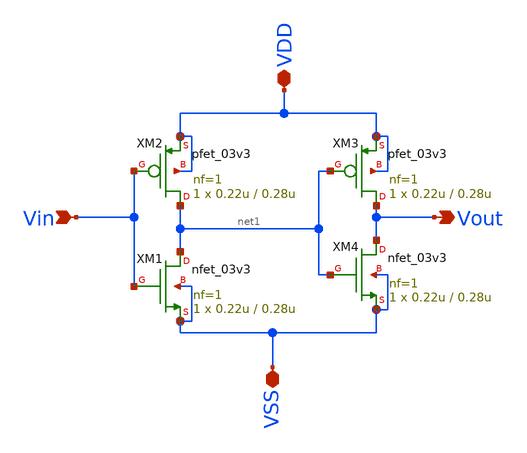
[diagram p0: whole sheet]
** sch_path: analog/top/buffer.sch
**.subckt buffer Vin Vout VSS VDD
*.ipin Vin
*.opin Vout
*.iopin VSS
*.iopin VDD
XM1 net1 Vin VSS VSS nfet_03v3 L=0.28u W=0.22u nf=1 ad='int((nf+1)/2) * W/nf * 0.18u' as='int((nf+2)/2) * W/nf * 0.18u'
+ pd='2*int((nf+1)/2) * (W/nf + 0.18u)' ps='2*int((nf+2)/2) * (W/nf + 0.18u)' nrd='0.18u / W' nrs='0.18u / W'
+ sa=0 sb=0 sd=0 m=1
XM2 net1 Vin VDD VDD pfet_03v3 L=0.28u W=0.22u nf=1 ad='int((nf+1)/2) * W/nf * 0.18u' as='int((nf+2)/2) * W/nf * 0.18u'
+ pd='2*int((nf+1)/2) * (W/nf + 0.18u)' ps='2*int((nf+2)/2) * (W/nf + 0.18u)' nrd='0.18u / W' nrs='0.18u / W'
+ sa=0 sb=0 sd=0 m=1
XM3 Vout net1 VDD VDD pfet_03v3 L=0.28u W=0.22u nf=1 ad='int((nf+1)/2) * W/nf * 0.18u' as='int((nf+2)/2) * W/nf * 0.18u'
+ pd='2*int((nf+1)/2) * (W/nf + 0.18u)' ps='2*int((nf+2)/2) * (W/nf + 0.18u)' nrd='0.18u / W' nrs='0.18u / W'
+ sa=0 sb=0 sd=0 m=1
XM4 Vout net1 VSS VSS nfet_03v3 L=0.28u W=0.22u nf=1 ad='int((nf+1)/2) * W/nf * 0.18u' as='int((nf+2)/2) * W/nf * 0.18u'
+ pd='2*int((nf+1)/2) * (W/nf + 0.18u)' ps='2*int((nf+2)/2) * (W/nf + 0.18u)' nrd='0.18u / W' nrs='0.18u / W'
+ sa=0 sb=0 sd=0 m=1
**.ends
.end
